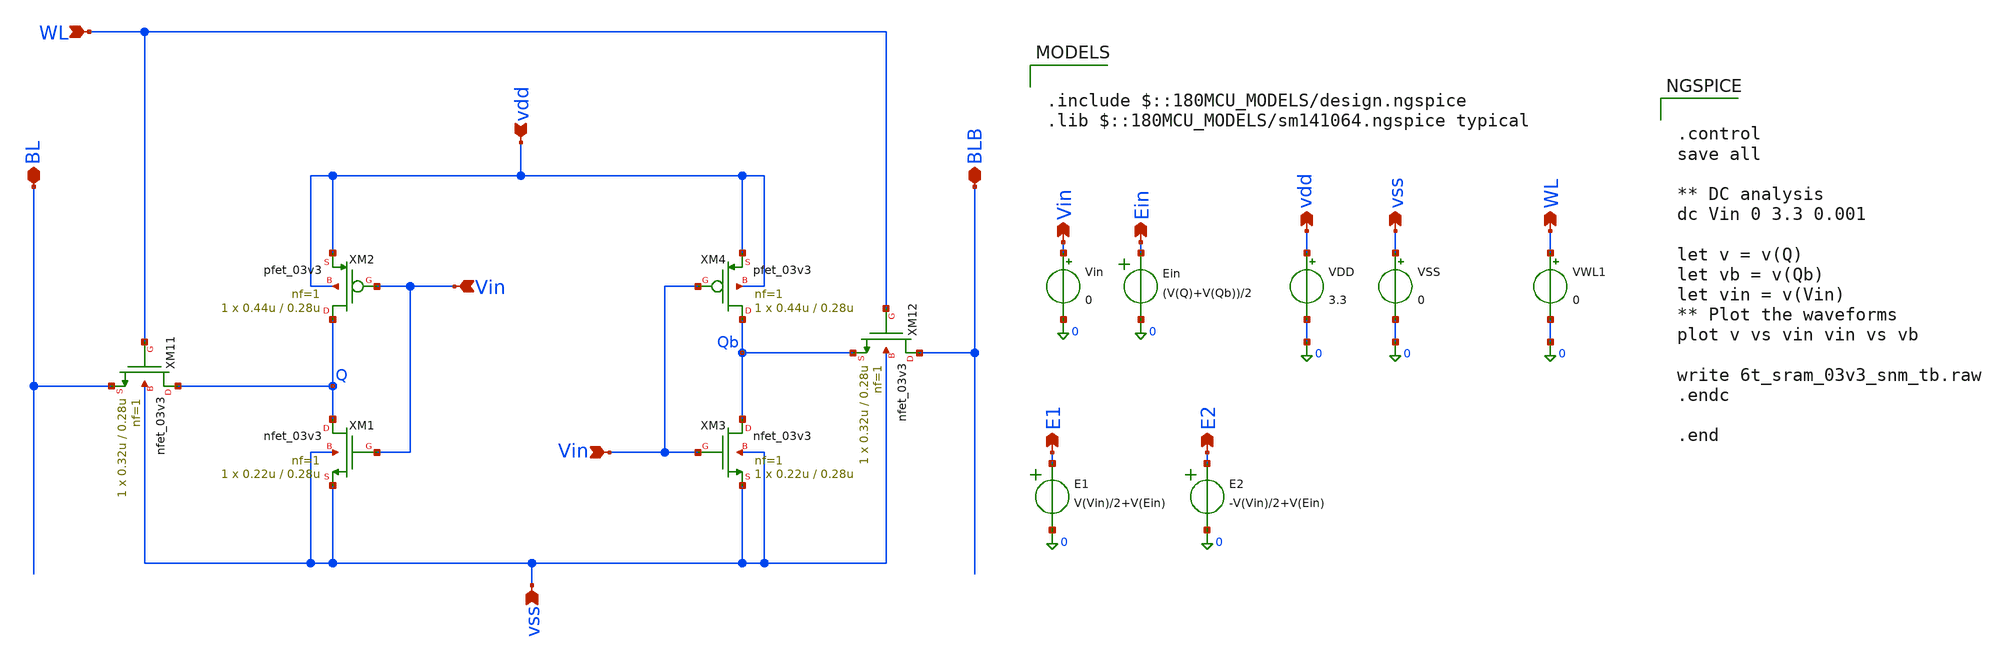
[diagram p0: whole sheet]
** sch_path: sim/analog/6t_sram_03v3_snm_tb.sch
**.subckt 6t_sram_03v3_snm_tb vdd vss vdd vss Vin Vin BL WL BLB WL E1 E2 Ein Vin
*.ipin vdd
*.ipin vss
*.opin vdd
*.opin vss
*.opin Vin
*.ipin Vin
*.iopin BL
*.ipin WL
*.iopin BLB
*.opin WL
*.opin E1
*.opin E2
*.opin Ein
*.ipin Vin
XM1 Q Vin vss vss nfet_03v3 L=0.28u W=0.22u nf=1 ad='int((nf+1)/2) * W/nf * 0.18u' as='int((nf+2)/2) * W/nf * 0.18u'
+ pd='2*int((nf+1)/2) * (W/nf + 0.18u)' ps='2*int((nf+2)/2) * (W/nf + 0.18u)' nrd='0.18u / W' nrs='0.18u / W'
+ sa=0 sb=0 sd=0 m=1
XM2 Q Vin vdd vdd pfet_03v3 L=0.28u W=0.44u nf=1 ad='int((nf+1)/2) * W/nf * 0.18u' as='int((nf+2)/2) * W/nf * 0.18u'
+ pd='2*int((nf+1)/2) * (W/nf + 0.18u)' ps='2*int((nf+2)/2) * (W/nf + 0.18u)' nrd='0.18u / W' nrs='0.18u / W'
+ sa=0 sb=0 sd=0 m=1
XM3 Qb Vin vss vss nfet_03v3 L=0.28u W=0.22u nf=1 ad='int((nf+1)/2) * W/nf * 0.18u' as='int((nf+2)/2) * W/nf * 0.18u'
+ pd='2*int((nf+1)/2) * (W/nf + 0.18u)' ps='2*int((nf+2)/2) * (W/nf + 0.18u)' nrd='0.18u / W' nrs='0.18u / W'
+ sa=0 sb=0 sd=0 m=1
XM4 Qb Vin vdd vdd pfet_03v3 L=0.28u W=0.44u nf=1 ad='int((nf+1)/2) * W/nf * 0.18u' as='int((nf+2)/2) * W/nf * 0.18u'
+ pd='2*int((nf+1)/2) * (W/nf + 0.18u)' ps='2*int((nf+2)/2) * (W/nf + 0.18u)' nrd='0.18u / W' nrs='0.18u / W'
+ sa=0 sb=0 sd=0 m=1
VDD vdd 0 3.3
VSS vss 0 0
Vin Vin 0 0
XM11 Q WL BL vss nfet_03v3 L=0.28u W=0.32u nf=1 ad='int((nf+1)/2) * W/nf * 0.18u' as='int((nf+2)/2) * W/nf * 0.18u'
+ pd='2*int((nf+1)/2) * (W/nf + 0.18u)' ps='2*int((nf+2)/2) * (W/nf + 0.18u)' nrd='0.18u / W' nrs='0.18u / W'
+ sa=0 sb=0 sd=0 m=1
XM12 BLB WL Qb vss nfet_03v3 L=0.28u W=0.32u nf=1 ad='int((nf+1)/2) * W/nf * 0.18u' as='int((nf+2)/2) * W/nf * 0.18u'
+ pd='2*int((nf+1)/2) * (W/nf + 0.18u)' ps='2*int((nf+2)/2) * (W/nf + 0.18u)' nrd='0.18u / W' nrs='0.18u / W'
+ sa=0 sb=0 sd=0 m=1
VWL1 WL 0 0
E1 E1 0 VOL=' V(Vin)/2+V(Ein) '
E2 E2 0 VOL=' -V(Vin)/2+V(Ein) '
Ein Ein 0 VOL=' (V(Q)+V(Qb))/2 '
**** begin user architecture code

.include $::180MCU_MODELS/design.ngspice
.lib $::180MCU_MODELS/sm141064.ngspice typical



.control
save all

** DC analysis
dc Vin 0 3.3 0.001

let v = v(Q)
let vb = v(Qb)
let vin = v(Vin)
** Plot the waveforms
plot v vs vin vin vs vb

write 6t_sram_03v3_snm_tb.raw
.endc

.end


**** end user architecture code
**.ends
.end
